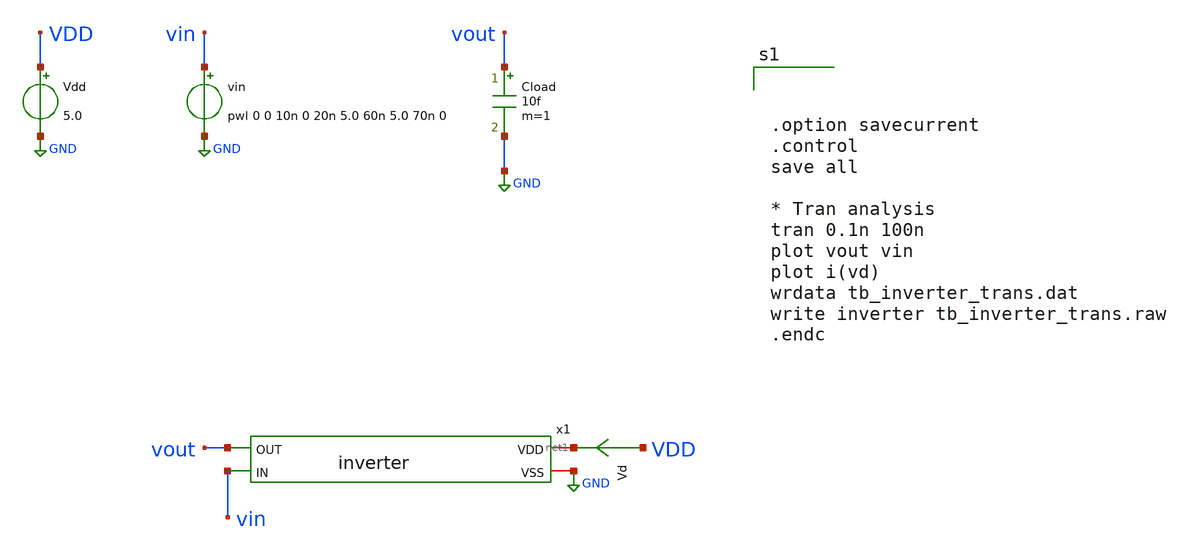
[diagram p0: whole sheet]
** sch_path: member_project/inverter/RISE-A/7158918/tb_inverter_trans.sch
**.subckt tb_inverter_trans
Vdd VDD GND 5.0
Vd VDD net1 0
.save i(vd)
vin vin GND pwl 0 0 10n 0 20n 5.0 60n 5.0 70n 0
x1 net1 vout vin GND inverter
Cload vout GND 10f m=1
**** begin user architecture code



.option savecurrent
.control
save all

* Tran analysis
tran 0.1n 100n
plot vout vin
plot i(vd)
wrdata tb_inverter_trans.dat
write inverter tb_inverter_trans.raw
.endc




 .include $::LIB/ip62_models
**** end user architecture code
**.ends

* expanding   symbol:  inverter.sym # of pins=4
** sym_path: member_project/inverter/RISE-A/7158918/inverter.sym
** sch_path: member_project/inverter/RISE-A/7158918/inverter.sch
.subckt inverter VDD OUT IN VSS
*.ipin OUT
*.ipin IN
*.iopin VDD
*.iopin VSS
XXM1 OUT IN VDD VDD PMOS w=3.4u l=1u nrd=0 nrs=0 m=1
XXM2 OUT IN VSS VSS NMOS w=3.4u l=1u nrd=0 nrs=0 m=1
.ends

.GLOBAL GND
.end
